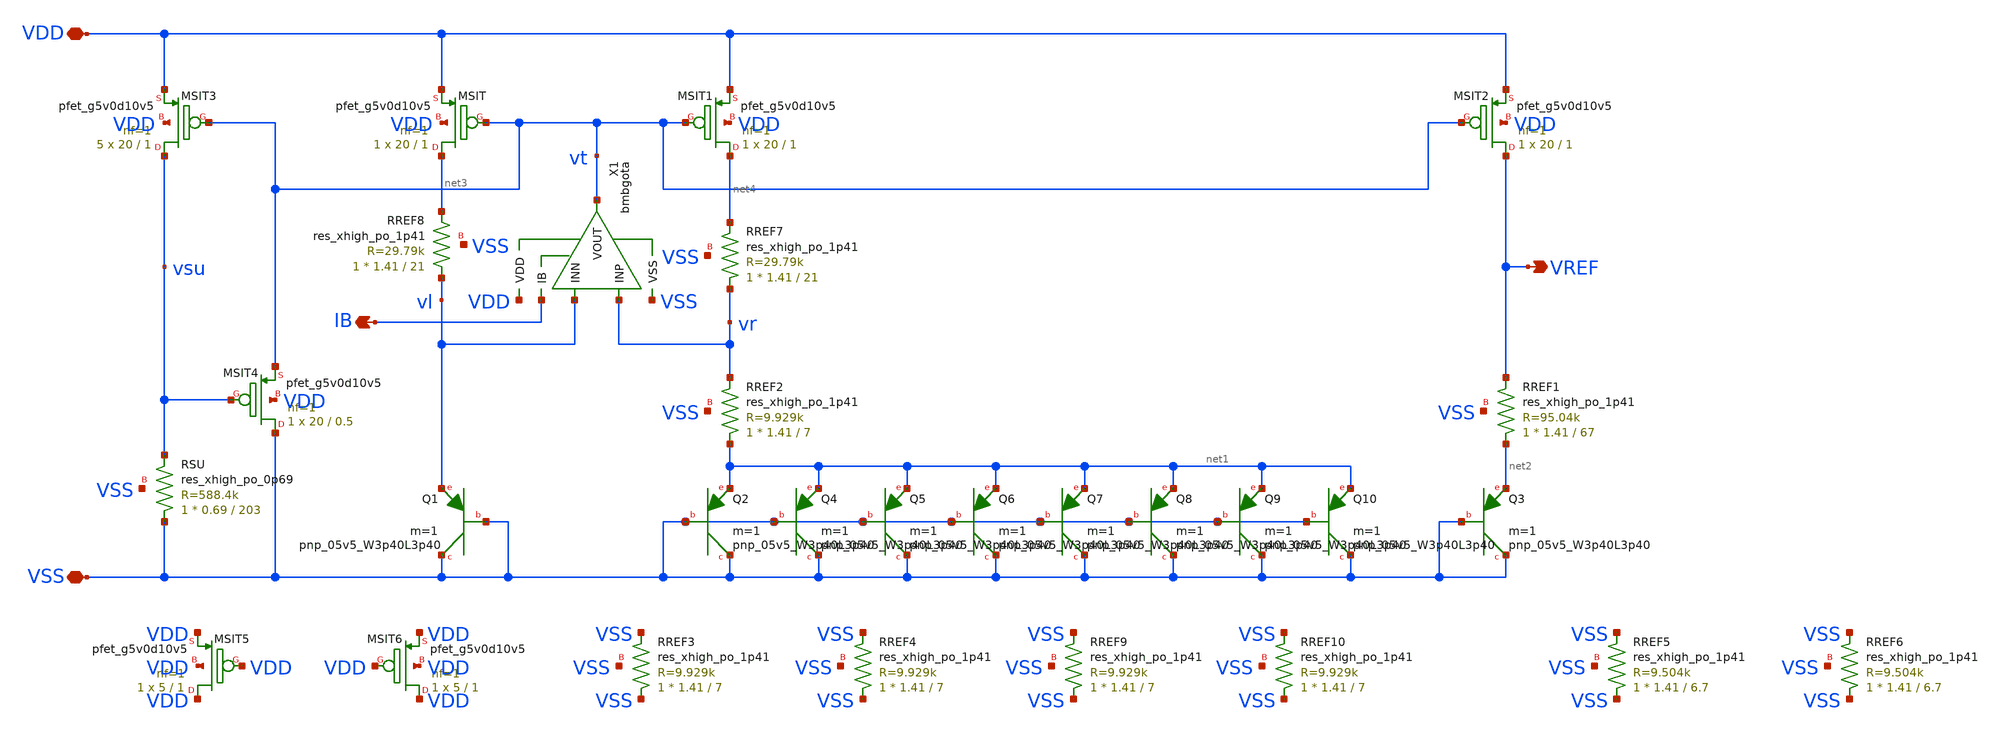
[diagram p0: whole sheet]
** sch_path: tt08/ip/bmbg/xschem/bmbg.sch
**.subckt bmbg VSS VDD VREF IB
*.iopin VSS
*.iopin VDD
*.opin VREF
*.opin IB
XMSIT net3 vt VDD VDD sky130_fd_pr__pfet_g5v0d10v5 L=1 W=20 nf=1 ad='int((nf+1)/2) * W/nf * 0.29' as='int((nf+2)/2) * W/nf * 0.29'
+ pd='2*int((nf+1)/2) * (W/nf + 0.29)' ps='2*int((nf+2)/2) * (W/nf + 0.29)' nrd='0.29 / W' nrs='0.29 / W'
+ sa=0 sb=0 sd=0 mult=1 m=1
XQ1 VSS VSS vl sky130_fd_pr__pnp_05v5_W3p40L3p40 m=1
XQ2 VSS VSS net1 sky130_fd_pr__pnp_05v5_W3p40L3p40 m=1
X1 VDD VSS vt IB vl vr bmbgota
XMSIT1 net4 vt VDD VDD sky130_fd_pr__pfet_g5v0d10v5 L=1 W=20 nf=1 ad='int((nf+1)/2) * W/nf * 0.29' as='int((nf+2)/2) * W/nf * 0.29'
+ pd='2*int((nf+1)/2) * (W/nf + 0.29)' ps='2*int((nf+2)/2) * (W/nf + 0.29)' nrd='0.29 / W' nrs='0.29 / W'
+ sa=0 sb=0 sd=0 mult=1 m=1
XQ3 VSS VSS net2 sky130_fd_pr__pnp_05v5_W3p40L3p40 m=1
XMSIT2 VREF vt VDD VDD sky130_fd_pr__pfet_g5v0d10v5 L=1 W=20 nf=1 ad='int((nf+1)/2) * W/nf * 0.29' as='int((nf+2)/2) * W/nf * 0.29'
+ pd='2*int((nf+1)/2) * (W/nf + 0.29)' ps='2*int((nf+2)/2) * (W/nf + 0.29)' nrd='0.29 / W' nrs='0.29 / W'
+ sa=0 sb=0 sd=0 mult=1 m=1
XQ4 VSS VSS net1 sky130_fd_pr__pnp_05v5_W3p40L3p40 m=1
XQ5 VSS VSS net1 sky130_fd_pr__pnp_05v5_W3p40L3p40 m=1
XQ6 VSS VSS net1 sky130_fd_pr__pnp_05v5_W3p40L3p40 m=1
XQ7 VSS VSS net1 sky130_fd_pr__pnp_05v5_W3p40L3p40 m=1
XQ8 VSS VSS net1 sky130_fd_pr__pnp_05v5_W3p40L3p40 m=1
XQ9 VSS VSS net1 sky130_fd_pr__pnp_05v5_W3p40L3p40 m=1
XQ10 VSS VSS net1 sky130_fd_pr__pnp_05v5_W3p40L3p40 m=1
XRREF1 net2 VREF VSS sky130_fd_pr__res_xhigh_po_1p41 L=67 mult=1 m=1
XRREF2 net1 vr VSS sky130_fd_pr__res_xhigh_po_1p41 L=7 mult=1 m=1
XRSU VSS vsu VSS sky130_fd_pr__res_xhigh_po_0p69 L=203 mult=1 m=1
XMSIT3 vsu vt VDD VDD sky130_fd_pr__pfet_g5v0d10v5 L=1 W=20 nf=1 ad='int((nf+1)/2) * W/nf * 0.29' as='int((nf+2)/2) * W/nf * 0.29'
+ pd='2*int((nf+1)/2) * (W/nf + 0.29)' ps='2*int((nf+2)/2) * (W/nf + 0.29)' nrd='0.29 / W' nrs='0.29 / W'
+ sa=0 sb=0 sd=0 mult=5 m=5
XMSIT4 VSS vsu vt VDD sky130_fd_pr__pfet_g5v0d10v5 L=0.5 W=20 nf=1 ad='int((nf+1)/2) * W/nf * 0.29' as='int((nf+2)/2) * W/nf * 0.29'
+ pd='2*int((nf+1)/2) * (W/nf + 0.29)' ps='2*int((nf+2)/2) * (W/nf + 0.29)' nrd='0.29 / W' nrs='0.29 / W'
+ sa=0 sb=0 sd=0 mult=1 m=1
XRREF3 VSS VSS VSS sky130_fd_pr__res_xhigh_po_1p41 L=7 mult=1 m=1
XRREF4 VSS VSS VSS sky130_fd_pr__res_xhigh_po_1p41 L=7 mult=1 m=1
XRREF5 VSS VSS VSS sky130_fd_pr__res_xhigh_po_1p41 L=6.7 mult=1 m=1
XRREF6 VSS VSS VSS sky130_fd_pr__res_xhigh_po_1p41 L=6.7 mult=1 m=1
XMSIT5 VDD VDD VDD VDD sky130_fd_pr__pfet_g5v0d10v5 L=1 W=5 nf=1 ad='int((nf+1)/2) * W/nf * 0.29' as='int((nf+2)/2) * W/nf * 0.29'
+ pd='2*int((nf+1)/2) * (W/nf + 0.29)' ps='2*int((nf+2)/2) * (W/nf + 0.29)' nrd='0.29 / W' nrs='0.29 / W'
+ sa=0 sb=0 sd=0 mult=1 m=1
XMSIT6 VDD VDD VDD VDD sky130_fd_pr__pfet_g5v0d10v5 L=1 W=5 nf=1 ad='int((nf+1)/2) * W/nf * 0.29' as='int((nf+2)/2) * W/nf * 0.29'
+ pd='2*int((nf+1)/2) * (W/nf + 0.29)' ps='2*int((nf+2)/2) * (W/nf + 0.29)' nrd='0.29 / W' nrs='0.29 / W'
+ sa=0 sb=0 sd=0 mult=1 m=1
XRREF7 vr net4 VSS sky130_fd_pr__res_xhigh_po_1p41 L=21 mult=1 m=1
XRREF8 vl net3 VSS sky130_fd_pr__res_xhigh_po_1p41 L=21 mult=1 m=1
XRREF9 VSS VSS VSS sky130_fd_pr__res_xhigh_po_1p41 L=7 mult=1 m=1
XRREF10 VSS VSS VSS sky130_fd_pr__res_xhigh_po_1p41 L=7 mult=1 m=1
**.ends

* expanding   symbol:  bmbgota.sym # of pins=6
** sym_path: bmbgota.sym
** sch_path: bmbgota.sch
.subckt bmbgota VDD VSS VOUT IB INN INP
*.iopin INP
*.iopin INN
*.iopin VOUT
*.opin IB
*.iopin VDD
*.iopin VSS
XMDR vr INP vt VDD sky130_fd_pr__pfet_g5v0d10v5 L=1 W=20 nf=1 ad='int((nf+1)/2) * W/nf * 0.29' as='int((nf+2)/2) * W/nf * 0.29'
+ pd='2*int((nf+1)/2) * (W/nf + 0.29)' ps='2*int((nf+2)/2) * (W/nf + 0.29)' nrd='0.29 / W' nrs='0.29 / W'
+ sa=0 sb=0 sd=0 mult=8 m=8
XMMIRL vl vl VSS VSS sky130_fd_pr__nfet_g5v0d10v5 L=2 W=5 nf=1 ad='int((nf+1)/2) * W/nf * 0.29' as='int((nf+2)/2) * W/nf * 0.29'
+ pd='2*int((nf+1)/2) * (W/nf + 0.29)' ps='2*int((nf+2)/2) * (W/nf + 0.29)' nrd='0.29 / W' nrs='0.29 / W'
+ sa=0 sb=0 sd=0 mult=4 m=4
XMMIRR vr vl VSS VSS sky130_fd_pr__nfet_g5v0d10v5 L=2 W=5 nf=1 ad='int((nf+1)/2) * W/nf * 0.29' as='int((nf+2)/2) * W/nf * 0.29'
+ pd='2*int((nf+1)/2) * (W/nf + 0.29)' ps='2*int((nf+2)/2) * (W/nf + 0.29)' nrd='0.29 / W' nrs='0.29 / W'
+ sa=0 sb=0 sd=0 mult=4 m=4
XMDL vl INN vt VDD sky130_fd_pr__pfet_g5v0d10v5 L=1 W=20 nf=1 ad='int((nf+1)/2) * W/nf * 0.29' as='int((nf+2)/2) * W/nf * 0.29'
+ pd='2*int((nf+1)/2) * (W/nf + 0.29)' ps='2*int((nf+2)/2) * (W/nf + 0.29)' nrd='0.29 / W' nrs='0.29 / W'
+ sa=0 sb=0 sd=0 mult=8 m=8
XMMIR2 vt IB VDD VDD sky130_fd_pr__pfet_g5v0d10v5 L=2 W=5 nf=1 ad='int((nf+1)/2) * W/nf * 0.29' as='int((nf+2)/2) * W/nf * 0.29'
+ pd='2*int((nf+1)/2) * (W/nf + 0.29)' ps='2*int((nf+2)/2) * (W/nf + 0.29)' nrd='0.29 / W' nrs='0.29 / W'
+ sa=0 sb=0 sd=0 mult=2 m=2
XMMIR1 IB IB VDD VDD sky130_fd_pr__pfet_g5v0d10v5 L=2 W=5 nf=1 ad='int((nf+1)/2) * W/nf * 0.29' as='int((nf+2)/2) * W/nf * 0.29'
+ pd='2*int((nf+1)/2) * (W/nf + 0.29)' ps='2*int((nf+2)/2) * (W/nf + 0.29)' nrd='0.29 / W' nrs='0.29 / W'
+ sa=0 sb=0 sd=0 mult=1 m=1
XMO VOUT vr VSS VSS sky130_fd_pr__nfet_g5v0d10v5 L=2 W=5 nf=1 ad='int((nf+1)/2) * W/nf * 0.29' as='int((nf+2)/2) * W/nf * 0.29'
+ pd='2*int((nf+1)/2) * (W/nf + 0.29)' ps='2*int((nf+2)/2) * (W/nf + 0.29)' nrd='0.29 / W' nrs='0.29 / W'
+ sa=0 sb=0 sd=0 mult=4 m=4
XMMIR3 VOUT IB VDD VDD sky130_fd_pr__pfet_g5v0d10v5 L=2 W=5 nf=1 ad='int((nf+1)/2) * W/nf * 0.29' as='int((nf+2)/2) * W/nf * 0.29'
+ pd='2*int((nf+1)/2) * (W/nf + 0.29)' ps='2*int((nf+2)/2) * (W/nf + 0.29)' nrd='0.29 / W' nrs='0.29 / W'
+ sa=0 sb=0 sd=0 mult=3 m=3
XR1 net1 vr VSS sky130_fd_pr__res_xhigh_po_1p41 L=7 mult=1 m=1
XC1 net1 VOUT sky130_fd_pr__cap_mim_m3_1 W=16 L=30 MF=1 m=1
XMDL1 VDD VDD VDD VDD sky130_fd_pr__pfet_g5v0d10v5 L=1 W=20 nf=1 ad='int((nf+1)/2) * W/nf * 0.29' as='int((nf+2)/2) * W/nf * 0.29'
+ pd='2*int((nf+1)/2) * (W/nf + 0.29)' ps='2*int((nf+2)/2) * (W/nf + 0.29)' nrd='0.29 / W' nrs='0.29 / W'
+ sa=0 sb=0 sd=0 mult=1 m=1
XMDR1 VDD VDD VDD VDD sky130_fd_pr__pfet_g5v0d10v5 L=1 W=20 nf=1 ad='int((nf+1)/2) * W/nf * 0.29' as='int((nf+2)/2) * W/nf * 0.29'
+ pd='2*int((nf+1)/2) * (W/nf + 0.29)' ps='2*int((nf+2)/2) * (W/nf + 0.29)' nrd='0.29 / W' nrs='0.29 / W'
+ sa=0 sb=0 sd=0 mult=1 m=1
XMMIRL1 VSS VSS VSS VSS sky130_fd_pr__nfet_g5v0d10v5 L=2 W=5 nf=1 ad='int((nf+1)/2) * W/nf * 0.29' as='int((nf+2)/2) * W/nf * 0.29'
+ pd='2*int((nf+1)/2) * (W/nf + 0.29)' ps='2*int((nf+2)/2) * (W/nf + 0.29)' nrd='0.29 / W' nrs='0.29 / W'
+ sa=0 sb=0 sd=0 mult=1 m=1
XMMIRR1 VSS VSS VSS VSS sky130_fd_pr__nfet_g5v0d10v5 L=2 W=5 nf=1 ad='int((nf+1)/2) * W/nf * 0.29' as='int((nf+2)/2) * W/nf * 0.29'
+ pd='2*int((nf+1)/2) * (W/nf + 0.29)' ps='2*int((nf+2)/2) * (W/nf + 0.29)' nrd='0.29 / W' nrs='0.29 / W'
+ sa=0 sb=0 sd=0 mult=1 m=1
.ends

.end
